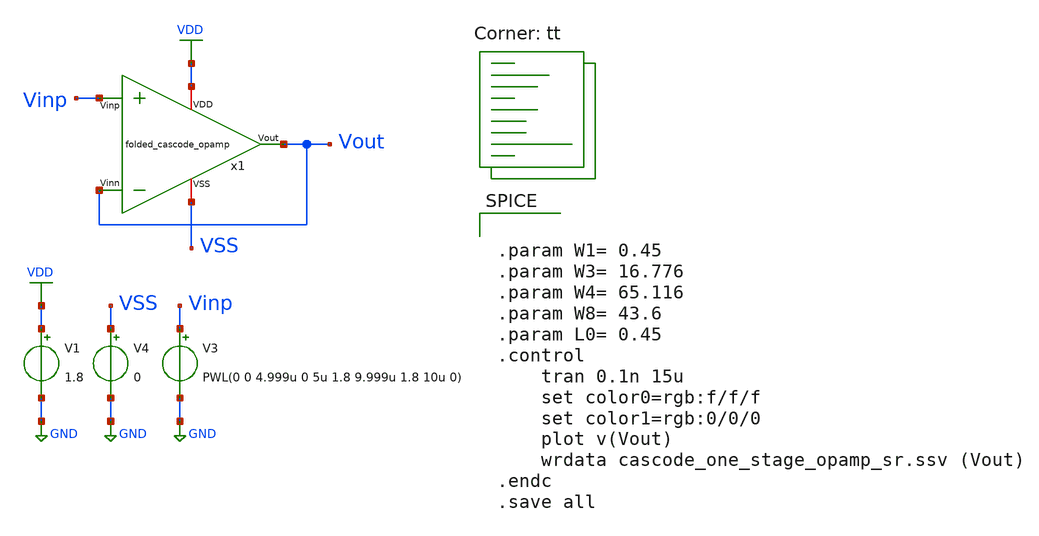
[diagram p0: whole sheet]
** sch_path: opamp_design/folded_cascode_opamp/folded_one_stage_opamp_sr.sch
**.subckt folded_one_stage_opamp_sr
V1 VDD GND 1.8
V3 Vinp GND PWL(0 0 4.999u 0 5u 1.8 9.999u 1.8 10u 0)
V4 VSS GND 0
x1 VDD Vout Vinp Vout VSS folded_cascode_opamp
**** begin user architecture code


.param W1= 0.45
.param W3= 16.776
.param W4= 65.116
.param W8= 43.6
.param L0= 0.45
.control
	tran 0.1n 15u
	set color0=rgb:f/f/f
	set color1=rgb:0/0/0
	plot v(Vout)
	wrdata cascode_one_stage_opamp_sr.ssv (Vout)
.endc
.save all


.lib $::SKYWATER_MODELS/sky130.lib.spice tt
**** end user architecture code
**.ends

* expanding   symbol:
*+  /home/ricardoatt/RATT_repos/Proyectos_xschem/opamp_design/folded_cascode_opamp/folded_cascode_opamp.sym # of pins=5
** sym_path: opamp_design/folded_cascode_opamp/folded_cascode_opamp.sym
** sch_path: opamp_design/folded_cascode_opamp/folded_cascode_opamp.sch
.subckt folded_cascode_opamp VDD Vout Vinp Vinn VSS
*.opin Vout
*.ipin Vinn
*.ipin Vinp
*.iopin VDD
*.iopin VSS
XM11 net4 net2 VSS VSS sky130_fd_pr__nfet_01v8 L={L0} W={W8} nf=1 ad='int((nf+1)/2) * W/nf * 0.29' as='int((nf+2)/2) * W/nf * 0.29'
+ pd='2*int((nf+1)/2) * (W/nf + 0.29)' ps='2*int((nf+2)/2) * (W/nf + 0.29)' nrd='0.29 / W' nrs='0.29 / W'
+ sa=0 sb=0 sd=0 mult=1 m=1
XM10 net3 net2 VSS VSS sky130_fd_pr__nfet_01v8 L={L0} W={W8} nf=1 ad='int((nf+1)/2) * W/nf * 0.29' as='int((nf+2)/2) * W/nf * 0.29'
+ pd='2*int((nf+1)/2) * (W/nf + 0.29)' ps='2*int((nf+2)/2) * (W/nf + 0.29)' nrd='0.29 / W' nrs='0.29 / W'
+ sa=0 sb=0 sd=0 mult=1 m=1
XM8 net2 net1 net3 VSS sky130_fd_pr__nfet_01v8 L={L0} W={W8} nf=1 ad='int((nf+1)/2) * W/nf * 0.29' as='int((nf+2)/2) * W/nf * 0.29'
+ pd='2*int((nf+1)/2) * (W/nf + 0.29)' ps='2*int((nf+2)/2) * (W/nf + 0.29)' nrd='0.29 / W' nrs='0.29 / W'
+ sa=0 sb=0 sd=0 mult=1 m=1
XM9 Vout net1 net4 VSS sky130_fd_pr__nfet_01v8 L={L0} W={W8} nf=1 ad='int((nf+1)/2) * W/nf * 0.29' as='int((nf+2)/2) * W/nf * 0.29'
+ pd='2*int((nf+1)/2) * (W/nf + 0.29)' ps='2*int((nf+2)/2) * (W/nf + 0.29)' nrd='0.29 / W' nrs='0.29 / W'
+ sa=0 sb=0 sd=0 mult=1 m=1
XM7 Vout net5 net8 VDD sky130_fd_pr__pfet_01v8 L={L0} W={W4} nf=1 ad='int((nf+1)/2) * W/nf * 0.29' as='int((nf+2)/2) * W/nf * 0.29'
+ pd='2*int((nf+1)/2) * (W/nf + 0.29)' ps='2*int((nf+2)/2) * (W/nf + 0.29)' nrd='0.29 / W' nrs='0.29 / W'
+ sa=0 sb=0 sd=0 mult=1 m=1
XM6 net2 net5 net7 VDD sky130_fd_pr__pfet_01v8 L={L0} W={W4} nf=1 ad='int((nf+1)/2) * W/nf * 0.29' as='int((nf+2)/2) * W/nf * 0.29'
+ pd='2*int((nf+1)/2) * (W/nf + 0.29)' ps='2*int((nf+2)/2) * (W/nf + 0.29)' nrd='0.29 / W' nrs='0.29 / W'
+ sa=0 sb=0 sd=0 mult=1 m=1
XM1 net7 Vinp net6 VSS sky130_fd_pr__nfet_01v8 L={L0} W={W1} nf=1 ad='int((nf+1)/2) * W/nf * 0.29' as='int((nf+2)/2) * W/nf * 0.29'
+ pd='2*int((nf+1)/2) * (W/nf + 0.29)' ps='2*int((nf+2)/2) * (W/nf + 0.29)' nrd='0.29 / W' nrs='0.29 / W'
+ sa=0 sb=0 sd=0 mult=1 m=1
XM2 net8 Vinn net6 VSS sky130_fd_pr__nfet_01v8 L={L0} W={W1} nf=1 ad='int((nf+1)/2) * W/nf * 0.29' as='int((nf+2)/2) * W/nf * 0.29'
+ pd='2*int((nf+1)/2) * (W/nf + 0.29)' ps='2*int((nf+2)/2) * (W/nf + 0.29)' nrd='0.29 / W' nrs='0.29 / W'
+ sa=0 sb=0 sd=0 mult=1 m=1
XM3 net6 net10 VSS VSS sky130_fd_pr__nfet_01v8 L={L0} W={W3} nf=1 ad='int((nf+1)/2) * W/nf * 0.29' as='int((nf+2)/2) * W/nf * 0.29'
+ pd='2*int((nf+1)/2) * (W/nf + 0.29)' ps='2*int((nf+2)/2) * (W/nf + 0.29)' nrd='0.29 / W' nrs='0.29 / W'
+ sa=0 sb=0 sd=0 mult=1 m=1
XM4 net7 net9 VDD VDD sky130_fd_pr__pfet_01v8 L={L0} W={W4} nf=1 ad='int((nf+1)/2) * W/nf * 0.29' as='int((nf+2)/2) * W/nf * 0.29'
+ pd='2*int((nf+1)/2) * (W/nf + 0.29)' ps='2*int((nf+2)/2) * (W/nf + 0.29)' nrd='0.29 / W' nrs='0.29 / W'
+ sa=0 sb=0 sd=0 mult=1 m=1
XM5 net8 net9 VDD VDD sky130_fd_pr__pfet_01v8 L={L0} W={W4} nf=1 ad='int((nf+1)/2) * W/nf * 0.29' as='int((nf+2)/2) * W/nf * 0.29'
+ pd='2*int((nf+1)/2) * (W/nf + 0.29)' ps='2*int((nf+2)/2) * (W/nf + 0.29)' nrd='0.29 / W' nrs='0.29 / W'
+ sa=0 sb=0 sd=0 mult=1 m=1
XM12 net9 net9 VDD VDD sky130_fd_pr__pfet_01v8 L={L0} W={W4} nf=1 ad='int((nf+1)/2) * W/nf * 0.29' as='int((nf+2)/2) * W/nf * 0.29'
+ pd='2*int((nf+1)/2) * (W/nf + 0.29)' ps='2*int((nf+2)/2) * (W/nf + 0.29)' nrd='0.29 / W' nrs='0.29 / W'
+ sa=0 sb=0 sd=0 mult=1 m=1
I4 net9 VSS 165u
XM13 net5 net5 VDD VDD sky130_fd_pr__pfet_01v8 L={L0} W={W4} nf=1 ad='int((nf+1)/2) * W/nf * 0.29' as='int((nf+2)/2) * W/nf * 0.29'
+ pd='2*int((nf+1)/2) * (W/nf + 0.29)' ps='2*int((nf+2)/2) * (W/nf + 0.29)' nrd='0.29 / W' nrs='0.29 / W'
+ sa=0 sb=0 sd=0 mult=1 m=1
I1 net5 VSS 165u
XM14 net1 net1 VSS VSS sky130_fd_pr__nfet_01v8 L={L0} W={W8} nf=1 ad='int((nf+1)/2) * W/nf * 0.29' as='int((nf+2)/2) * W/nf * 0.29'
+ pd='2*int((nf+1)/2) * (W/nf + 0.29)' ps='2*int((nf+2)/2) * (W/nf + 0.29)' nrd='0.29 / W' nrs='0.29 / W'
+ sa=0 sb=0 sd=0 mult=1 m=1
I2 VDD net1 165u
XM15 net10 net10 VSS VSS sky130_fd_pr__nfet_01v8 L={L0} W={W3} nf=1 ad='int((nf+1)/2) * W/nf * 0.29'
+ as='int((nf+2)/2) * W/nf * 0.29' pd='2*int((nf+1)/2) * (W/nf + 0.29)' ps='2*int((nf+2)/2) * (W/nf + 0.29)'
+ nrd='0.29 / W' nrs='0.29 / W' sa=0 sb=0 sd=0 mult=1 m=1
I3 VDD net10 150u
.ends

.GLOBAL VDD
.GLOBAL GND
.end
